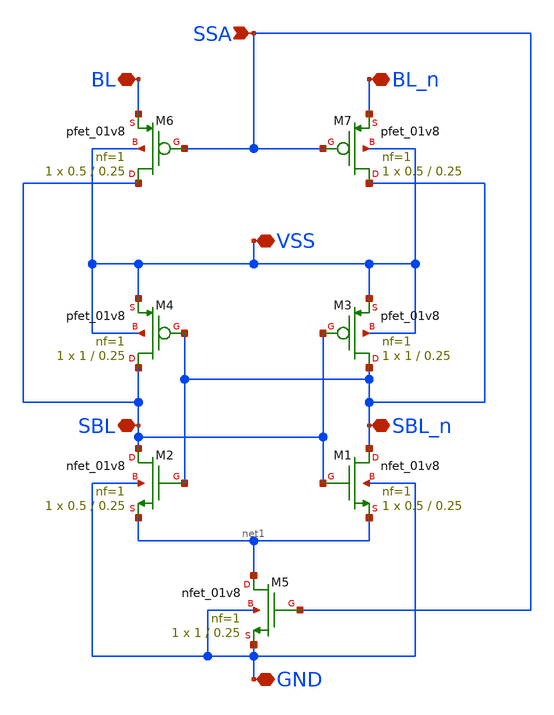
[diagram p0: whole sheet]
** sch_path: ISOsense_amp.sch
**.subckt ISOsense_amp VSS BL_n BL GND SSA SBL SBL_n
*.iopin VSS
*.iopin BL_n
*.iopin BL
*.iopin GND
*.ipin SSA
*.iopin SBL
*.iopin SBL_n
XM1 SBL_n SBL net1 GND sky130_fd_pr__nfet_01v8 L=0.25 W=0.5 nf=1 ad='int((nf+1)/2) * W/nf * 0.29' as='int((nf+2)/2) * W/nf * 0.29'
+ pd='2*int((nf+1)/2) * (W/nf + 0.29)' ps='2*int((nf+2)/2) * (W/nf + 0.29)' nrd='0.29 / W' nrs='0.29 / W'
+ sa=0 sb=0 sd=0 mult=1 m=1
XM2 SBL SBL_n net1 GND sky130_fd_pr__nfet_01v8 L=0.25 W=0.5 nf=1 ad='int((nf+1)/2) * W/nf * 0.29' as='int((nf+2)/2) * W/nf * 0.29'
+ pd='2*int((nf+1)/2) * (W/nf + 0.29)' ps='2*int((nf+2)/2) * (W/nf + 0.29)' nrd='0.29 / W' nrs='0.29 / W'
+ sa=0 sb=0 sd=0 mult=1 m=1
XM3 SBL_n SBL VSS VSS sky130_fd_pr__pfet_01v8 L=0.25 W=1 nf=1 ad='int((nf+1)/2) * W/nf * 0.29' as='int((nf+2)/2) * W/nf * 0.29'
+ pd='2*int((nf+1)/2) * (W/nf + 0.29)' ps='2*int((nf+2)/2) * (W/nf + 0.29)' nrd='0.29 / W' nrs='0.29 / W'
+ sa=0 sb=0 sd=0 mult=1 m=1
XM4 SBL SBL_n VSS VSS sky130_fd_pr__pfet_01v8 L=0.25 W=1 nf=1 ad='int((nf+1)/2) * W/nf * 0.29' as='int((nf+2)/2) * W/nf * 0.29'
+ pd='2*int((nf+1)/2) * (W/nf + 0.29)' ps='2*int((nf+2)/2) * (W/nf + 0.29)' nrd='0.29 / W' nrs='0.29 / W'
+ sa=0 sb=0 sd=0 mult=1 m=1
XM5 net1 SSA GND GND sky130_fd_pr__nfet_01v8 L=0.25 W=1 nf=1 ad='int((nf+1)/2) * W/nf * 0.29' as='int((nf+2)/2) * W/nf * 0.29'
+ pd='2*int((nf+1)/2) * (W/nf + 0.29)' ps='2*int((nf+2)/2) * (W/nf + 0.29)' nrd='0.29 / W' nrs='0.29 / W'
+ sa=0 sb=0 sd=0 mult=1 m=1
XM6 SBL SSA BL VSS sky130_fd_pr__pfet_01v8 L=0.25 W=0.5 nf=1 ad='int((nf+1)/2) * W/nf * 0.29' as='int((nf+2)/2) * W/nf * 0.29'
+ pd='2*int((nf+1)/2) * (W/nf + 0.29)' ps='2*int((nf+2)/2) * (W/nf + 0.29)' nrd='0.29 / W' nrs='0.29 / W'
+ sa=0 sb=0 sd=0 mult=1 m=1
XM7 SBL_n SSA BL_n VSS sky130_fd_pr__pfet_01v8 L=0.25 W=0.5 nf=1 ad='int((nf+1)/2) * W/nf * 0.29' as='int((nf+2)/2) * W/nf * 0.29'
+ pd='2*int((nf+1)/2) * (W/nf + 0.29)' ps='2*int((nf+2)/2) * (W/nf + 0.29)' nrd='0.29 / W' nrs='0.29 / W'
+ sa=0 sb=0 sd=0 mult=1 m=1
**.ends
.end
